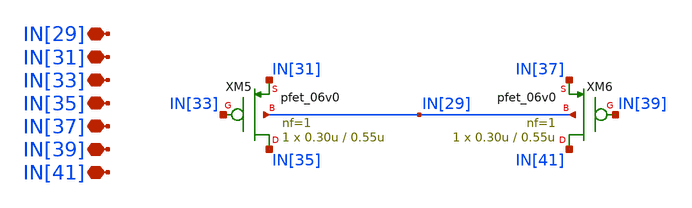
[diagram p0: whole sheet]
** sch_path: designs/libs/core_single-fet/pfet-pin/pfet-pin.sch
**.subckt pfet-pin IN[31] IN[29] IN[33] IN[35] IN[37] IN[39] IN[41]
*.iopin IN[31]
*.iopin IN[29]
*.iopin IN[33]
*.iopin IN[35]
*.iopin IN[37]
*.iopin IN[39]
*.iopin IN[41]
XM5 IN[35] IN[33] IN[31] IN[29] pfet_06v0 L=0.55u W=0.30u nf=1 ad='int((nf+1)/2) * W/nf * 0.18u' as='int((nf+2)/2) * W/nf * 0.18u'
+ pd='2*int((nf+1)/2) * (W/nf + 0.18u)' ps='2*int((nf+2)/2) * (W/nf + 0.18u)' nrd='0.18u / W' nrs='0.18u / W'
+ sa=0 sb=0 sd=0 m=1
XM6 IN[41] IN[39] IN[37] IN[29] pfet_06v0 L=0.55u W=0.30u nf=1 ad='int((nf+1)/2) * W/nf * 0.18u' as='int((nf+2)/2) * W/nf * 0.18u'
+ pd='2*int((nf+1)/2) * (W/nf + 0.18u)' ps='2*int((nf+2)/2) * (W/nf + 0.18u)' nrd='0.18u / W' nrs='0.18u / W'
+ sa=0 sb=0 sd=0 m=1
**.ends
.end
